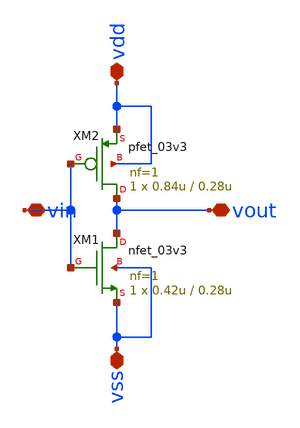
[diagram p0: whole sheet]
** sch_path: src/Pixel/inv.sch
**.subckt inv vin vout vdd vss
*.iopin vin
*.iopin vout
*.iopin vdd
*.iopin vss
XM1 vout vin vss vss nfet_03v3 L=0.28u W=0.42u nf=1 ad='int((nf+1)/2) * W/nf * 0.18u' as='int((nf+2)/2) * W/nf * 0.18u'
+ pd='2*int((nf+1)/2) * (W/nf + 0.18u)' ps='2*int((nf+2)/2) * (W/nf + 0.18u)' nrd='0.18u / W' nrs='0.18u / W'
+ sa=0 sb=0 sd=0 m=1
XM2 vout vin vdd vdd pfet_03v3 L=0.28u W=0.84u nf=1 ad='int((nf+1)/2) * W/nf * 0.18u' as='int((nf+2)/2) * W/nf * 0.18u'
+ pd='2*int((nf+1)/2) * (W/nf + 0.18u)' ps='2*int((nf+2)/2) * (W/nf + 0.18u)' nrd='0.18u / W' nrs='0.18u / W'
+ sa=0 sb=0 sd=0 m=1
**.ends
.end
